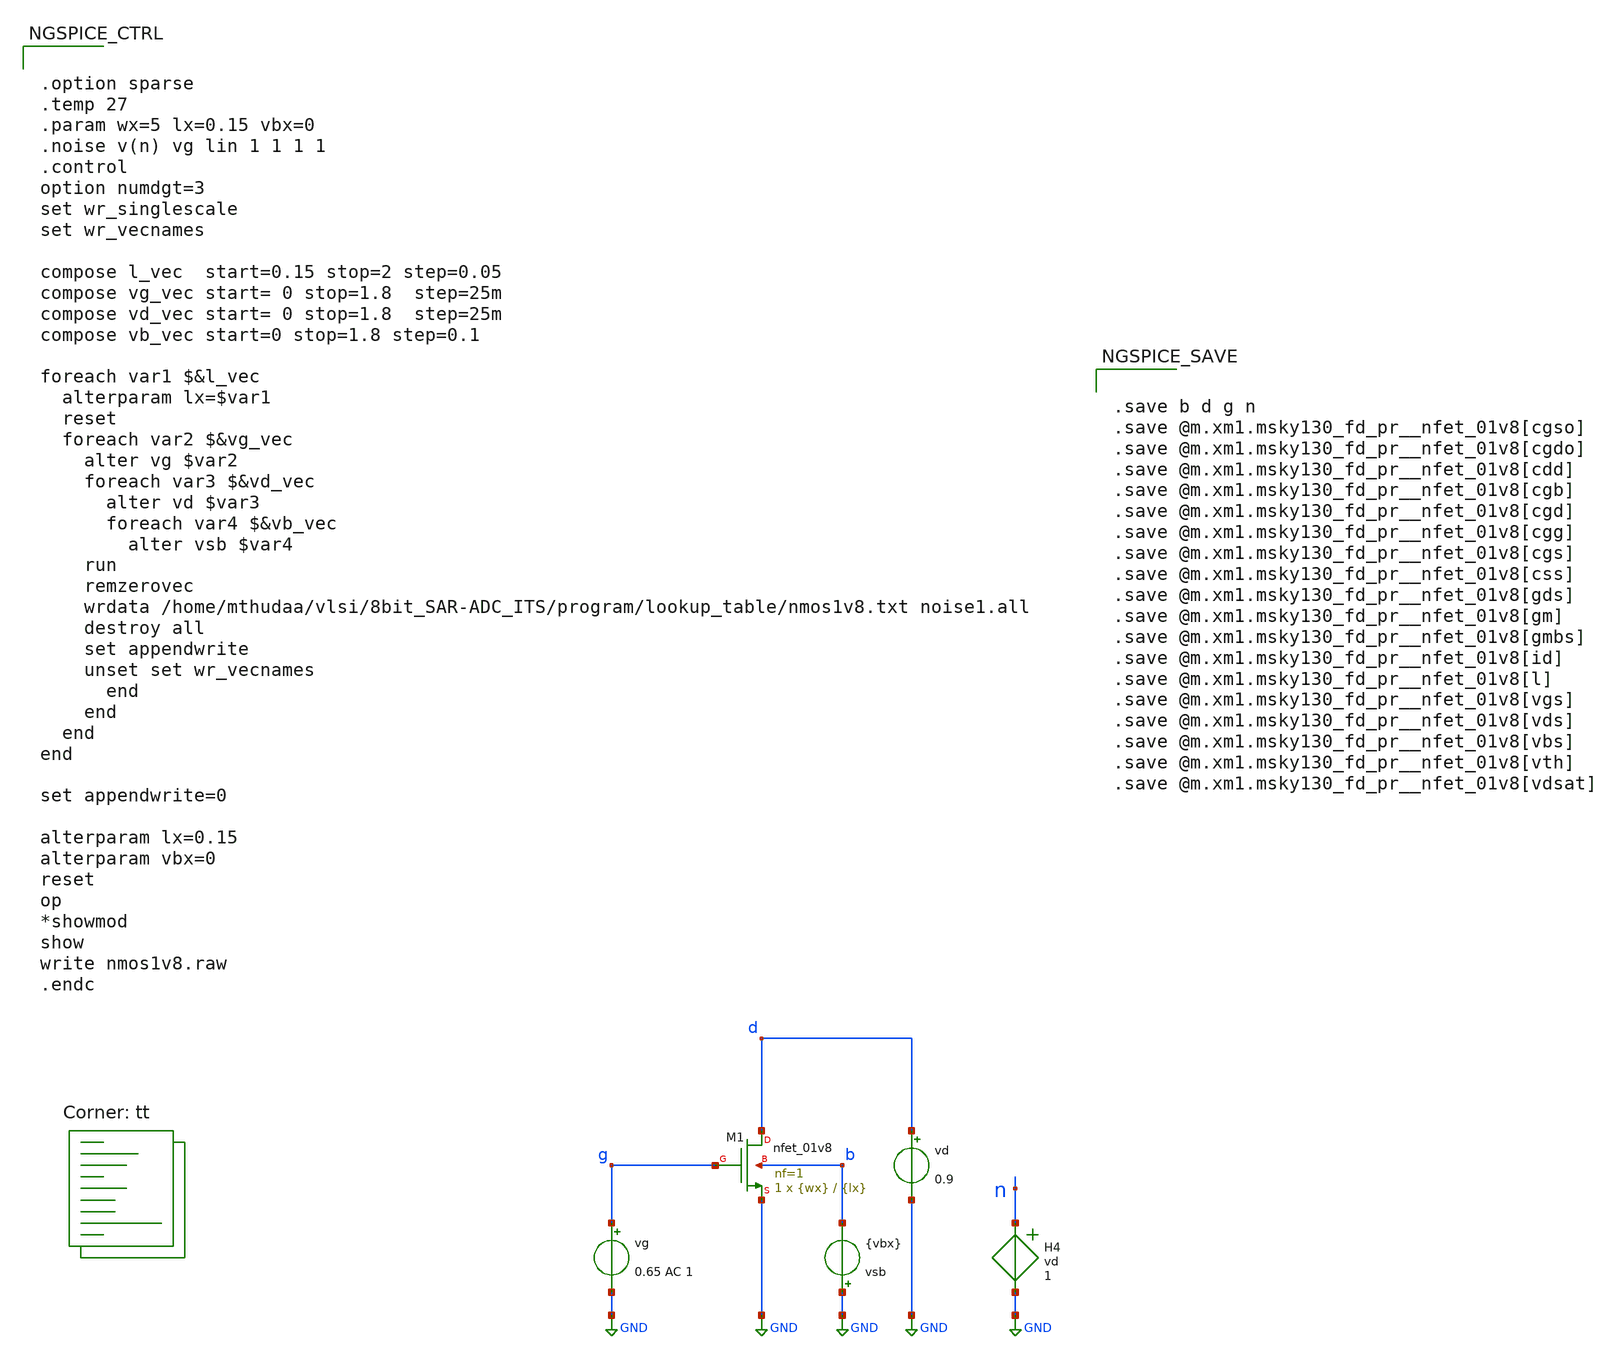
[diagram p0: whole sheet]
** sch_path: xschem/nmos1v8_sweep.sch
* (c) 2024 H. Pretl, Apache-2.0 license (adapted from B. Murmann)
**.subckt nmos1v8_sweep
vg g GND 0.65 AC 1
vd d GND 0.9
vsb GND b {vbx}
H4 n GND vd 1
XM1 d g GND b sky130_fd_pr__nfet_01v8 L={lx} W={wx} nf=1 ad='int((nf+1)/2) * W/nf * 0.29' as='int((nf+2)/2) * W/nf * 0.29'
+ pd='2*int((nf+1)/2) * (W/nf + 0.29)' ps='2*int((nf+2)/2) * (W/nf + 0.29)' nrd='0.29 / W' nrs='0.29 / W'
+ sa=0 sb=0 sd=0 mult=1 m=1
**** begin user architecture code


.option sparse
.temp 27
.param wx=5 lx=0.15 vbx=0
.noise v(n) vg lin 1 1 1 1
.control
option numdgt=3
set wr_singlescale
set wr_vecnames

compose l_vec  start=0.15 stop=2 step=0.05
compose vg_vec start= 0 stop=1.8  step=25m
compose vd_vec start= 0 stop=1.8  step=25m
compose vb_vec start=0 stop=1.8 step=0.1

foreach var1 $&l_vec
  alterparam lx=$var1
  reset
  foreach var2 $&vg_vec
    alter vg $var2
    foreach var3 $&vd_vec
      alter vd $var3
      foreach var4 $&vb_vec
        alter vsb $var4
	run
	remzerovec
	wrdata /home/mthudaa/vlsi/8bit_SAR-ADC_ITS/program/lookup_table/nmos1v8.txt noise1.all
	destroy all
	set appendwrite
	unset set wr_vecnames
      end
    end
  end
end

set appendwrite=0

alterparam lx=0.15
alterparam vbx=0
reset
op
*showmod
show
write nmos1v8.raw
.endc




.save b d g n
.save @m.xm1.msky130_fd_pr__nfet_01v8[cgso]
.save @m.xm1.msky130_fd_pr__nfet_01v8[cgdo]
.save @m.xm1.msky130_fd_pr__nfet_01v8[cdd]
.save @m.xm1.msky130_fd_pr__nfet_01v8[cgb]
.save @m.xm1.msky130_fd_pr__nfet_01v8[cgd]
.save @m.xm1.msky130_fd_pr__nfet_01v8[cgg]
.save @m.xm1.msky130_fd_pr__nfet_01v8[cgs]
.save @m.xm1.msky130_fd_pr__nfet_01v8[css]
.save @m.xm1.msky130_fd_pr__nfet_01v8[gds]
.save @m.xm1.msky130_fd_pr__nfet_01v8[gm]
.save @m.xm1.msky130_fd_pr__nfet_01v8[gmbs]
.save @m.xm1.msky130_fd_pr__nfet_01v8[id]
.save @m.xm1.msky130_fd_pr__nfet_01v8[l]
.save @m.xm1.msky130_fd_pr__nfet_01v8[vgs]
.save @m.xm1.msky130_fd_pr__nfet_01v8[vds]
.save @m.xm1.msky130_fd_pr__nfet_01v8[vbs]
.save @m.xm1.msky130_fd_pr__nfet_01v8[vth]
.save @m.xm1.msky130_fd_pr__nfet_01v8[vdsat]


.lib $::SKYWATER_MODELS/sky130.lib.spice tt
**** end user architecture code
**.ends
.GLOBAL GND
.end
